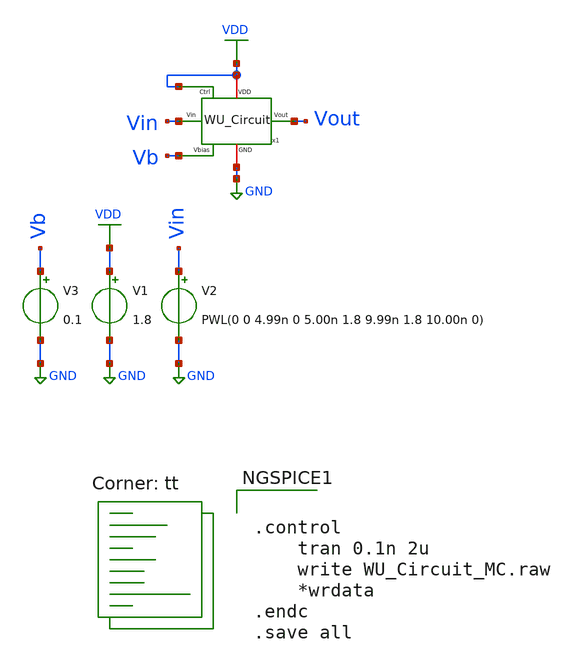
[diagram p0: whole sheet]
** sch_path: SNN/WU_Circuit_tb.sch
**.subckt WU_Circuit_tb
V1 VDD GND 1.8
V2 Vin GND PWL(0 0 4.99n 0 5.00n 1.8 9.99n 1.8 10.00n 0)
V3 Vb GND 0.1
x1 Vb VDD Vin GND VDD Vout WU_Circuit
**** begin user architecture code
.lib $::SKYWATER_MODELS/sky130.lib.spice tt


.control
	tran 0.1n 2u
	write WU_Circuit_MC.raw
	*wrdata
.endc
.save all


**** end user architecture code
**.ends
.GLOBAL GND
.GLOBAL VDD
.end
